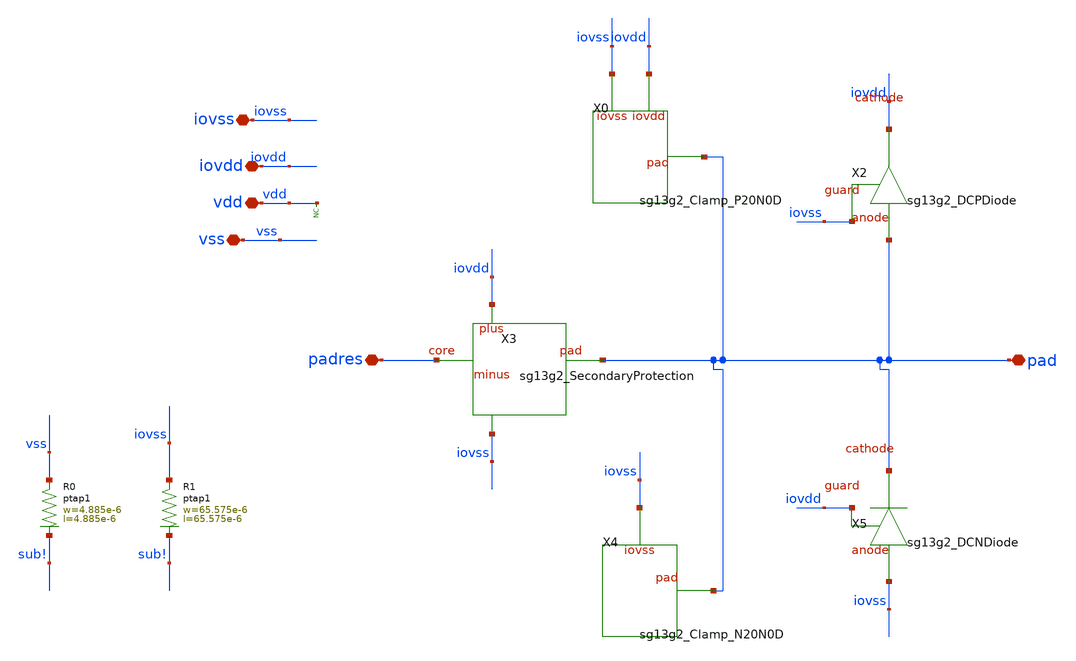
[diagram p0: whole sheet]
** sch_path: ihp-sg13g2/libs.ref/sg13g2_io/sch/xschem/sg13g2_IOPadAnalog.sch
**.subckt sg13g2_IOPadAnalog vdd vss iovdd padres pad iovss
*.iopin vdd
*.iopin vss
*.iopin iovdd
*.iopin padres
*.iopin pad
*.iopin iovss
* noconn vdd
X0 pad iovss iovdd sg13g2_Clamp_P20N0D
X2 iovss iovdd pad sg13g2_DCPDiode
X3 iovdd pad iovss padres sg13g2_SecondaryProtection
X4 pad iovss sg13g2_Clamp_N20N0D
X5 iovdd pad iovss sg13g2_DCNDiode
XR0 vss sub! ptap1 R=22.58 w=4.885e-6 l=4.885e-6
XR1 iovss sub! ptap1 R=214.8m w=65.575e-6 l=65.575e-6
**.ends
.end
